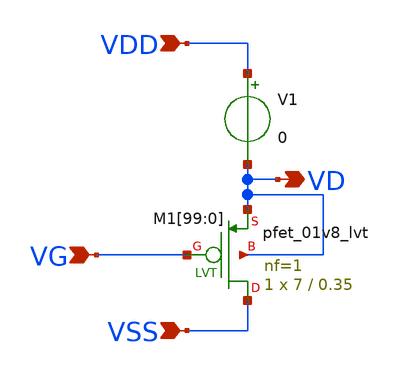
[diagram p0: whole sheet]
** sch_path: design/THESIS_EXP_RO_INVERTER_SKY130A/TB_FET.sch
**.subckt TB_FET VDD VSS VD VG
*.ipin VDD
*.ipin VSS
*.opin VD
*.ipin VG
V1 VDD VD 0
.save i(v1)
XM1[99] VSS VG VD VD sky130_fd_pr__pfet_01v8_lvt L=0.35 W=7 nf=1 ad='int((1 + 1)/2) * 7 / 1 * 0.29' as='int((1 + 2)/2) * 7 / 1 * 0.29'
+ pd='2*int((1 + 1)/2) * (7 / 1 + 0.29)' ps='2*int((1 + 2)/2) * (7 / 1 + 0.29)' nrd='0.29 / 7 ' nrs='0.29 / 7 '
+ sa=0 sb=0 sd=0 mult=1 m=1
XM1[98] VSS VG VD VD sky130_fd_pr__pfet_01v8_lvt L=0.35 W=7 nf=1 ad='int((1 + 1)/2) * 7 / 1 * 0.29' as='int((1 + 2)/2) * 7 / 1 * 0.29'
+ pd='2*int((1 + 1)/2) * (7 / 1 + 0.29)' ps='2*int((1 + 2)/2) * (7 / 1 + 0.29)' nrd='0.29 / 7 ' nrs='0.29 / 7 '
+ sa=0 sb=0 sd=0 mult=1 m=1
XM1[97] VSS VG VD VD sky130_fd_pr__pfet_01v8_lvt L=0.35 W=7 nf=1 ad='int((1 + 1)/2) * 7 / 1 * 0.29' as='int((1 + 2)/2) * 7 / 1 * 0.29'
+ pd='2*int((1 + 1)/2) * (7 / 1 + 0.29)' ps='2*int((1 + 2)/2) * (7 / 1 + 0.29)' nrd='0.29 / 7 ' nrs='0.29 / 7 '
+ sa=0 sb=0 sd=0 mult=1 m=1
XM1[96] VSS VG VD VD sky130_fd_pr__pfet_01v8_lvt L=0.35 W=7 nf=1 ad='int((1 + 1)/2) * 7 / 1 * 0.29' as='int((1 + 2)/2) * 7 / 1 * 0.29'
+ pd='2*int((1 + 1)/2) * (7 / 1 + 0.29)' ps='2*int((1 + 2)/2) * (7 / 1 + 0.29)' nrd='0.29 / 7 ' nrs='0.29 / 7 '
+ sa=0 sb=0 sd=0 mult=1 m=1
XM1[95] VSS VG VD VD sky130_fd_pr__pfet_01v8_lvt L=0.35 W=7 nf=1 ad='int((1 + 1)/2) * 7 / 1 * 0.29' as='int((1 + 2)/2) * 7 / 1 * 0.29'
+ pd='2*int((1 + 1)/2) * (7 / 1 + 0.29)' ps='2*int((1 + 2)/2) * (7 / 1 + 0.29)' nrd='0.29 / 7 ' nrs='0.29 / 7 '
+ sa=0 sb=0 sd=0 mult=1 m=1
XM1[94] VSS VG VD VD sky130_fd_pr__pfet_01v8_lvt L=0.35 W=7 nf=1 ad='int((1 + 1)/2) * 7 / 1 * 0.29' as='int((1 + 2)/2) * 7 / 1 * 0.29'
+ pd='2*int((1 + 1)/2) * (7 / 1 + 0.29)' ps='2*int((1 + 2)/2) * (7 / 1 + 0.29)' nrd='0.29 / 7 ' nrs='0.29 / 7 '
+ sa=0 sb=0 sd=0 mult=1 m=1
XM1[93] VSS VG VD VD sky130_fd_pr__pfet_01v8_lvt L=0.35 W=7 nf=1 ad='int((1 + 1)/2) * 7 / 1 * 0.29' as='int((1 + 2)/2) * 7 / 1 * 0.29'
+ pd='2*int((1 + 1)/2) * (7 / 1 + 0.29)' ps='2*int((1 + 2)/2) * (7 / 1 + 0.29)' nrd='0.29 / 7 ' nrs='0.29 / 7 '
+ sa=0 sb=0 sd=0 mult=1 m=1
XM1[92] VSS VG VD VD sky130_fd_pr__pfet_01v8_lvt L=0.35 W=7 nf=1 ad='int((1 + 1)/2) * 7 / 1 * 0.29' as='int((1 + 2)/2) * 7 / 1 * 0.29'
+ pd='2*int((1 + 1)/2) * (7 / 1 + 0.29)' ps='2*int((1 + 2)/2) * (7 / 1 + 0.29)' nrd='0.29 / 7 ' nrs='0.29 / 7 '
+ sa=0 sb=0 sd=0 mult=1 m=1
XM1[91] VSS VG VD VD sky130_fd_pr__pfet_01v8_lvt L=0.35 W=7 nf=1 ad='int((1 + 1)/2) * 7 / 1 * 0.29' as='int((1 + 2)/2) * 7 / 1 * 0.29'
+ pd='2*int((1 + 1)/2) * (7 / 1 + 0.29)' ps='2*int((1 + 2)/2) * (7 / 1 + 0.29)' nrd='0.29 / 7 ' nrs='0.29 / 7 '
+ sa=0 sb=0 sd=0 mult=1 m=1
XM1[90] VSS VG VD VD sky130_fd_pr__pfet_01v8_lvt L=0.35 W=7 nf=1 ad='int((1 + 1)/2) * 7 / 1 * 0.29' as='int((1 + 2)/2) * 7 / 1 * 0.29'
+ pd='2*int((1 + 1)/2) * (7 / 1 + 0.29)' ps='2*int((1 + 2)/2) * (7 / 1 + 0.29)' nrd='0.29 / 7 ' nrs='0.29 / 7 '
+ sa=0 sb=0 sd=0 mult=1 m=1
XM1[89] VSS VG VD VD sky130_fd_pr__pfet_01v8_lvt L=0.35 W=7 nf=1 ad='int((1 + 1)/2) * 7 / 1 * 0.29' as='int((1 + 2)/2) * 7 / 1 * 0.29'
+ pd='2*int((1 + 1)/2) * (7 / 1 + 0.29)' ps='2*int((1 + 2)/2) * (7 / 1 + 0.29)' nrd='0.29 / 7 ' nrs='0.29 / 7 '
+ sa=0 sb=0 sd=0 mult=1 m=1
XM1[88] VSS VG VD VD sky130_fd_pr__pfet_01v8_lvt L=0.35 W=7 nf=1 ad='int((1 + 1)/2) * 7 / 1 * 0.29' as='int((1 + 2)/2) * 7 / 1 * 0.29'
+ pd='2*int((1 + 1)/2) * (7 / 1 + 0.29)' ps='2*int((1 + 2)/2) * (7 / 1 + 0.29)' nrd='0.29 / 7 ' nrs='0.29 / 7 '
+ sa=0 sb=0 sd=0 mult=1 m=1
XM1[87] VSS VG VD VD sky130_fd_pr__pfet_01v8_lvt L=0.35 W=7 nf=1 ad='int((1 + 1)/2) * 7 / 1 * 0.29' as='int((1 + 2)/2) * 7 / 1 * 0.29'
+ pd='2*int((1 + 1)/2) * (7 / 1 + 0.29)' ps='2*int((1 + 2)/2) * (7 / 1 + 0.29)' nrd='0.29 / 7 ' nrs='0.29 / 7 '
+ sa=0 sb=0 sd=0 mult=1 m=1
XM1[86] VSS VG VD VD sky130_fd_pr__pfet_01v8_lvt L=0.35 W=7 nf=1 ad='int((1 + 1)/2) * 7 / 1 * 0.29' as='int((1 + 2)/2) * 7 / 1 * 0.29'
+ pd='2*int((1 + 1)/2) * (7 / 1 + 0.29)' ps='2*int((1 + 2)/2) * (7 / 1 + 0.29)' nrd='0.29 / 7 ' nrs='0.29 / 7 '
+ sa=0 sb=0 sd=0 mult=1 m=1
XM1[85] VSS VG VD VD sky130_fd_pr__pfet_01v8_lvt L=0.35 W=7 nf=1 ad='int((1 + 1)/2) * 7 / 1 * 0.29' as='int((1 + 2)/2) * 7 / 1 * 0.29'
+ pd='2*int((1 + 1)/2) * (7 / 1 + 0.29)' ps='2*int((1 + 2)/2) * (7 / 1 + 0.29)' nrd='0.29 / 7 ' nrs='0.29 / 7 '
+ sa=0 sb=0 sd=0 mult=1 m=1
XM1[84] VSS VG VD VD sky130_fd_pr__pfet_01v8_lvt L=0.35 W=7 nf=1 ad='int((1 + 1)/2) * 7 / 1 * 0.29' as='int((1 + 2)/2) * 7 / 1 * 0.29'
+ pd='2*int((1 + 1)/2) * (7 / 1 + 0.29)' ps='2*int((1 + 2)/2) * (7 / 1 + 0.29)' nrd='0.29 / 7 ' nrs='0.29 / 7 '
+ sa=0 sb=0 sd=0 mult=1 m=1
XM1[83] VSS VG VD VD sky130_fd_pr__pfet_01v8_lvt L=0.35 W=7 nf=1 ad='int((1 + 1)/2) * 7 / 1 * 0.29' as='int((1 + 2)/2) * 7 / 1 * 0.29'
+ pd='2*int((1 + 1)/2) * (7 / 1 + 0.29)' ps='2*int((1 + 2)/2) * (7 / 1 + 0.29)' nrd='0.29 / 7 ' nrs='0.29 / 7 '
+ sa=0 sb=0 sd=0 mult=1 m=1
XM1[82] VSS VG VD VD sky130_fd_pr__pfet_01v8_lvt L=0.35 W=7 nf=1 ad='int((1 + 1)/2) * 7 / 1 * 0.29' as='int((1 + 2)/2) * 7 / 1 * 0.29'
+ pd='2*int((1 + 1)/2) * (7 / 1 + 0.29)' ps='2*int((1 + 2)/2) * (7 / 1 + 0.29)' nrd='0.29 / 7 ' nrs='0.29 / 7 '
+ sa=0 sb=0 sd=0 mult=1 m=1
XM1[81] VSS VG VD VD sky130_fd_pr__pfet_01v8_lvt L=0.35 W=7 nf=1 ad='int((1 + 1)/2) * 7 / 1 * 0.29' as='int((1 + 2)/2) * 7 / 1 * 0.29'
+ pd='2*int((1 + 1)/2) * (7 / 1 + 0.29)' ps='2*int((1 + 2)/2) * (7 / 1 + 0.29)' nrd='0.29 / 7 ' nrs='0.29 / 7 '
+ sa=0 sb=0 sd=0 mult=1 m=1
XM1[80] VSS VG VD VD sky130_fd_pr__pfet_01v8_lvt L=0.35 W=7 nf=1 ad='int((1 + 1)/2) * 7 / 1 * 0.29' as='int((1 + 2)/2) * 7 / 1 * 0.29'
+ pd='2*int((1 + 1)/2) * (7 / 1 + 0.29)' ps='2*int((1 + 2)/2) * (7 / 1 + 0.29)' nrd='0.29 / 7 ' nrs='0.29 / 7 '
+ sa=0 sb=0 sd=0 mult=1 m=1
XM1[79] VSS VG VD VD sky130_fd_pr__pfet_01v8_lvt L=0.35 W=7 nf=1 ad='int((1 + 1)/2) * 7 / 1 * 0.29' as='int((1 + 2)/2) * 7 / 1 * 0.29'
+ pd='2*int((1 + 1)/2) * (7 / 1 + 0.29)' ps='2*int((1 + 2)/2) * (7 / 1 + 0.29)' nrd='0.29 / 7 ' nrs='0.29 / 7 '
+ sa=0 sb=0 sd=0 mult=1 m=1
XM1[78] VSS VG VD VD sky130_fd_pr__pfet_01v8_lvt L=0.35 W=7 nf=1 ad='int((1 + 1)/2) * 7 / 1 * 0.29' as='int((1 + 2)/2) * 7 / 1 * 0.29'
+ pd='2*int((1 + 1)/2) * (7 / 1 + 0.29)' ps='2*int((1 + 2)/2) * (7 / 1 + 0.29)' nrd='0.29 / 7 ' nrs='0.29 / 7 '
+ sa=0 sb=0 sd=0 mult=1 m=1
XM1[77] VSS VG VD VD sky130_fd_pr__pfet_01v8_lvt L=0.35 W=7 nf=1 ad='int((1 + 1)/2) * 7 / 1 * 0.29' as='int((1 + 2)/2) * 7 / 1 * 0.29'
+ pd='2*int((1 + 1)/2) * (7 / 1 + 0.29)' ps='2*int((1 + 2)/2) * (7 / 1 + 0.29)' nrd='0.29 / 7 ' nrs='0.29 / 7 '
+ sa=0 sb=0 sd=0 mult=1 m=1
XM1[76] VSS VG VD VD sky130_fd_pr__pfet_01v8_lvt L=0.35 W=7 nf=1 ad='int((1 + 1)/2) * 7 / 1 * 0.29' as='int((1 + 2)/2) * 7 / 1 * 0.29'
+ pd='2*int((1 + 1)/2) * (7 / 1 + 0.29)' ps='2*int((1 + 2)/2) * (7 / 1 + 0.29)' nrd='0.29 / 7 ' nrs='0.29 / 7 '
+ sa=0 sb=0 sd=0 mult=1 m=1
XM1[75] VSS VG VD VD sky130_fd_pr__pfet_01v8_lvt L=0.35 W=7 nf=1 ad='int((1 + 1)/2) * 7 / 1 * 0.29' as='int((1 + 2)/2) * 7 / 1 * 0.29'
+ pd='2*int((1 + 1)/2) * (7 / 1 + 0.29)' ps='2*int((1 + 2)/2) * (7 / 1 + 0.29)' nrd='0.29 / 7 ' nrs='0.29 / 7 '
+ sa=0 sb=0 sd=0 mult=1 m=1
XM1[74] VSS VG VD VD sky130_fd_pr__pfet_01v8_lvt L=0.35 W=7 nf=1 ad='int((1 + 1)/2) * 7 / 1 * 0.29' as='int((1 + 2)/2) * 7 / 1 * 0.29'
+ pd='2*int((1 + 1)/2) * (7 / 1 + 0.29)' ps='2*int((1 + 2)/2) * (7 / 1 + 0.29)' nrd='0.29 / 7 ' nrs='0.29 / 7 '
+ sa=0 sb=0 sd=0 mult=1 m=1
XM1[73] VSS VG VD VD sky130_fd_pr__pfet_01v8_lvt L=0.35 W=7 nf=1 ad='int((1 + 1)/2) * 7 / 1 * 0.29' as='int((1 + 2)/2) * 7 / 1 * 0.29'
+ pd='2*int((1 + 1)/2) * (7 / 1 + 0.29)' ps='2*int((1 + 2)/2) * (7 / 1 + 0.29)' nrd='0.29 / 7 ' nrs='0.29 / 7 '
+ sa=0 sb=0 sd=0 mult=1 m=1
XM1[72] VSS VG VD VD sky130_fd_pr__pfet_01v8_lvt L=0.35 W=7 nf=1 ad='int((1 + 1)/2) * 7 / 1 * 0.29' as='int((1 + 2)/2) * 7 / 1 * 0.29'
+ pd='2*int((1 + 1)/2) * (7 / 1 + 0.29)' ps='2*int((1 + 2)/2) * (7 / 1 + 0.29)' nrd='0.29 / 7 ' nrs='0.29 / 7 '
+ sa=0 sb=0 sd=0 mult=1 m=1
XM1[71] VSS VG VD VD sky130_fd_pr__pfet_01v8_lvt L=0.35 W=7 nf=1 ad='int((1 + 1)/2) * 7 / 1 * 0.29' as='int((1 + 2)/2) * 7 / 1 * 0.29'
+ pd='2*int((1 + 1)/2) * (7 / 1 + 0.29)' ps='2*int((1 + 2)/2) * (7 / 1 + 0.29)' nrd='0.29 / 7 ' nrs='0.29 / 7 '
+ sa=0 sb=0 sd=0 mult=1 m=1
XM1[70] VSS VG VD VD sky130_fd_pr__pfet_01v8_lvt L=0.35 W=7 nf=1 ad='int((1 + 1)/2) * 7 / 1 * 0.29' as='int((1 + 2)/2) * 7 / 1 * 0.29'
+ pd='2*int((1 + 1)/2) * (7 / 1 + 0.29)' ps='2*int((1 + 2)/2) * (7 / 1 + 0.29)' nrd='0.29 / 7 ' nrs='0.29 / 7 '
+ sa=0 sb=0 sd=0 mult=1 m=1
XM1[69] VSS VG VD VD sky130_fd_pr__pfet_01v8_lvt L=0.35 W=7 nf=1 ad='int((1 + 1)/2) * 7 / 1 * 0.29' as='int((1 + 2)/2) * 7 / 1 * 0.29'
+ pd='2*int((1 + 1)/2) * (7 / 1 + 0.29)' ps='2*int((1 + 2)/2) * (7 / 1 + 0.29)' nrd='0.29 / 7 ' nrs='0.29 / 7 '
+ sa=0 sb=0 sd=0 mult=1 m=1
XM1[68] VSS VG VD VD sky130_fd_pr__pfet_01v8_lvt L=0.35 W=7 nf=1 ad='int((1 + 1)/2) * 7 / 1 * 0.29' as='int((1 + 2)/2) * 7 / 1 * 0.29'
+ pd='2*int((1 + 1)/2) * (7 / 1 + 0.29)' ps='2*int((1 + 2)/2) * (7 / 1 + 0.29)' nrd='0.29 / 7 ' nrs='0.29 / 7 '
+ sa=0 sb=0 sd=0 mult=1 m=1
XM1[67] VSS VG VD VD sky130_fd_pr__pfet_01v8_lvt L=0.35 W=7 nf=1 ad='int((1 + 1)/2) * 7 / 1 * 0.29' as='int((1 + 2)/2) * 7 / 1 * 0.29'
+ pd='2*int((1 + 1)/2) * (7 / 1 + 0.29)' ps='2*int((1 + 2)/2) * (7 / 1 + 0.29)' nrd='0.29 / 7 ' nrs='0.29 / 7 '
+ sa=0 sb=0 sd=0 mult=1 m=1
XM1[66] VSS VG VD VD sky130_fd_pr__pfet_01v8_lvt L=0.35 W=7 nf=1 ad='int((1 + 1)/2) * 7 / 1 * 0.29' as='int((1 + 2)/2) * 7 / 1 * 0.29'
+ pd='2*int((1 + 1)/2) * (7 / 1 + 0.29)' ps='2*int((1 + 2)/2) * (7 / 1 + 0.29)' nrd='0.29 / 7 ' nrs='0.29 / 7 '
+ sa=0 sb=0 sd=0 mult=1 m=1
XM1[65] VSS VG VD VD sky130_fd_pr__pfet_01v8_lvt L=0.35 W=7 nf=1 ad='int((1 + 1)/2) * 7 / 1 * 0.29' as='int((1 + 2)/2) * 7 / 1 * 0.29'
+ pd='2*int((1 + 1)/2) * (7 / 1 + 0.29)' ps='2*int((1 + 2)/2) * (7 / 1 + 0.29)' nrd='0.29 / 7 ' nrs='0.29 / 7 '
+ sa=0 sb=0 sd=0 mult=1 m=1
XM1[64] VSS VG VD VD sky130_fd_pr__pfet_01v8_lvt L=0.35 W=7 nf=1 ad='int((1 + 1)/2) * 7 / 1 * 0.29' as='int((1 + 2)/2) * 7 / 1 * 0.29'
+ pd='2*int((1 + 1)/2) * (7 / 1 + 0.29)' ps='2*int((1 + 2)/2) * (7 / 1 + 0.29)' nrd='0.29 / 7 ' nrs='0.29 / 7 '
+ sa=0 sb=0 sd=0 mult=1 m=1
XM1[63] VSS VG VD VD sky130_fd_pr__pfet_01v8_lvt L=0.35 W=7 nf=1 ad='int((1 + 1)/2) * 7 / 1 * 0.29' as='int((1 + 2)/2) * 7 / 1 * 0.29'
+ pd='2*int((1 + 1)/2) * (7 / 1 + 0.29)' ps='2*int((1 + 2)/2) * (7 / 1 + 0.29)' nrd='0.29 / 7 ' nrs='0.29 / 7 '
+ sa=0 sb=0 sd=0 mult=1 m=1
XM1[62] VSS VG VD VD sky130_fd_pr__pfet_01v8_lvt L=0.35 W=7 nf=1 ad='int((1 + 1)/2) * 7 / 1 * 0.29' as='int((1 + 2)/2) * 7 / 1 * 0.29'
+ pd='2*int((1 + 1)/2) * (7 / 1 + 0.29)' ps='2*int((1 + 2)/2) * (7 / 1 + 0.29)' nrd='0.29 / 7 ' nrs='0.29 / 7 '
+ sa=0 sb=0 sd=0 mult=1 m=1
XM1[61] VSS VG VD VD sky130_fd_pr__pfet_01v8_lvt L=0.35 W=7 nf=1 ad='int((1 + 1)/2) * 7 / 1 * 0.29' as='int((1 + 2)/2) * 7 / 1 * 0.29'
+ pd='2*int((1 + 1)/2) * (7 / 1 + 0.29)' ps='2*int((1 + 2)/2) * (7 / 1 + 0.29)' nrd='0.29 / 7 ' nrs='0.29 / 7 '
+ sa=0 sb=0 sd=0 mult=1 m=1
XM1[60] VSS VG VD VD sky130_fd_pr__pfet_01v8_lvt L=0.35 W=7 nf=1 ad='int((1 + 1)/2) * 7 / 1 * 0.29' as='int((1 + 2)/2) * 7 / 1 * 0.29'
+ pd='2*int((1 + 1)/2) * (7 / 1 + 0.29)' ps='2*int((1 + 2)/2) * (7 / 1 + 0.29)' nrd='0.29 / 7 ' nrs='0.29 / 7 '
+ sa=0 sb=0 sd=0 mult=1 m=1
XM1[59] VSS VG VD VD sky130_fd_pr__pfet_01v8_lvt L=0.35 W=7 nf=1 ad='int((1 + 1)/2) * 7 / 1 * 0.29' as='int((1 + 2)/2) * 7 / 1 * 0.29'
+ pd='2*int((1 + 1)/2) * (7 / 1 + 0.29)' ps='2*int((1 + 2)/2) * (7 / 1 + 0.29)' nrd='0.29 / 7 ' nrs='0.29 / 7 '
+ sa=0 sb=0 sd=0 mult=1 m=1
XM1[58] VSS VG VD VD sky130_fd_pr__pfet_01v8_lvt L=0.35 W=7 nf=1 ad='int((1 + 1)/2) * 7 / 1 * 0.29' as='int((1 + 2)/2) * 7 / 1 * 0.29'
+ pd='2*int((1 + 1)/2) * (7 / 1 + 0.29)' ps='2*int((1 + 2)/2) * (7 / 1 + 0.29)' nrd='0.29 / 7 ' nrs='0.29 / 7 '
+ sa=0 sb=0 sd=0 mult=1 m=1
XM1[57] VSS VG VD VD sky130_fd_pr__pfet_01v8_lvt L=0.35 W=7 nf=1 ad='int((1 + 1)/2) * 7 / 1 * 0.29' as='int((1 + 2)/2) * 7 / 1 * 0.29'
+ pd='2*int((1 + 1)/2) * (7 / 1 + 0.29)' ps='2*int((1 + 2)/2) * (7 / 1 + 0.29)' nrd='0.29 / 7 ' nrs='0.29 / 7 '
+ sa=0 sb=0 sd=0 mult=1 m=1
XM1[56] VSS VG VD VD sky130_fd_pr__pfet_01v8_lvt L=0.35 W=7 nf=1 ad='int((1 + 1)/2) * 7 / 1 * 0.29' as='int((1 + 2)/2) * 7 / 1 * 0.29'
+ pd='2*int((1 + 1)/2) * (7 / 1 + 0.29)' ps='2*int((1 + 2)/2) * (7 / 1 + 0.29)' nrd='0.29 / 7 ' nrs='0.29 / 7 '
+ sa=0 sb=0 sd=0 mult=1 m=1
XM1[55] VSS VG VD VD sky130_fd_pr__pfet_01v8_lvt L=0.35 W=7 nf=1 ad='int((1 + 1)/2) * 7 / 1 * 0.29' as='int((1 + 2)/2) * 7 / 1 * 0.29'
+ pd='2*int((1 + 1)/2) * (7 / 1 + 0.29)' ps='2*int((1 + 2)/2) * (7 / 1 + 0.29)' nrd='0.29 / 7 ' nrs='0.29 / 7 '
+ sa=0 sb=0 sd=0 mult=1 m=1
XM1[54] VSS VG VD VD sky130_fd_pr__pfet_01v8_lvt L=0.35 W=7 nf=1 ad='int((1 + 1)/2) * 7 / 1 * 0.29' as='int((1 + 2)/2) * 7 / 1 * 0.29'
+ pd='2*int((1 + 1)/2) * (7 / 1 + 0.29)' ps='2*int((1 + 2)/2) * (7 / 1 + 0.29)' nrd='0.29 / 7 ' nrs='0.29 / 7 '
+ sa=0 sb=0 sd=0 mult=1 m=1
XM1[53] VSS VG VD VD sky130_fd_pr__pfet_01v8_lvt L=0.35 W=7 nf=1 ad='int((1 + 1)/2) * 7 / 1 * 0.29' as='int((1 + 2)/2) * 7 / 1 * 0.29'
+ pd='2*int((1 + 1)/2) * (7 / 1 + 0.29)' ps='2*int((1 + 2)/2) * (7 / 1 + 0.29)' nrd='0.29 / 7 ' nrs='0.29 / 7 '
+ sa=0 sb=0 sd=0 mult=1 m=1
XM1[52] VSS VG VD VD sky130_fd_pr__pfet_01v8_lvt L=0.35 W=7 nf=1 ad='int((1 + 1)/2) * 7 / 1 * 0.29' as='int((1 + 2)/2) * 7 / 1 * 0.29'
+ pd='2*int((1 + 1)/2) * (7 / 1 + 0.29)' ps='2*int((1 + 2)/2) * (7 / 1 + 0.29)' nrd='0.29 / 7 ' nrs='0.29 / 7 '
+ sa=0 sb=0 sd=0 mult=1 m=1
XM1[51] VSS VG VD VD sky130_fd_pr__pfet_01v8_lvt L=0.35 W=7 nf=1 ad='int((1 + 1)/2) * 7 / 1 * 0.29' as='int((1 + 2)/2) * 7 / 1 * 0.29'
+ pd='2*int((1 + 1)/2) * (7 / 1 + 0.29)' ps='2*int((1 + 2)/2) * (7 / 1 + 0.29)' nrd='0.29 / 7 ' nrs='0.29 / 7 '
+ sa=0 sb=0 sd=0 mult=1 m=1
XM1[50] VSS VG VD VD sky130_fd_pr__pfet_01v8_lvt L=0.35 W=7 nf=1 ad='int((1 + 1)/2) * 7 / 1 * 0.29' as='int((1 + 2)/2) * 7 / 1 * 0.29'
+ pd='2*int((1 + 1)/2) * (7 / 1 + 0.29)' ps='2*int((1 + 2)/2) * (7 / 1 + 0.29)' nrd='0.29 / 7 ' nrs='0.29 / 7 '
+ sa=0 sb=0 sd=0 mult=1 m=1
XM1[49] VSS VG VD VD sky130_fd_pr__pfet_01v8_lvt L=0.35 W=7 nf=1 ad='int((1 + 1)/2) * 7 / 1 * 0.29' as='int((1 + 2)/2) * 7 / 1 * 0.29'
+ pd='2*int((1 + 1)/2) * (7 / 1 + 0.29)' ps='2*int((1 + 2)/2) * (7 / 1 + 0.29)' nrd='0.29 / 7 ' nrs='0.29 / 7 '
+ sa=0 sb=0 sd=0 mult=1 m=1
XM1[48] VSS VG VD VD sky130_fd_pr__pfet_01v8_lvt L=0.35 W=7 nf=1 ad='int((1 + 1)/2) * 7 / 1 * 0.29' as='int((1 + 2)/2) * 7 / 1 * 0.29'
+ pd='2*int((1 + 1)/2) * (7 / 1 + 0.29)' ps='2*int((1 + 2)/2) * (7 / 1 + 0.29)' nrd='0.29 / 7 ' nrs='0.29 / 7 '
+ sa=0 sb=0 sd=0 mult=1 m=1
XM1[47] VSS VG VD VD sky130_fd_pr__pfet_01v8_lvt L=0.35 W=7 nf=1 ad='int((1 + 1)/2) * 7 / 1 * 0.29' as='int((1 + 2)/2) * 7 / 1 * 0.29'
+ pd='2*int((1 + 1)/2) * (7 / 1 + 0.29)' ps='2*int((1 + 2)/2) * (7 / 1 + 0.29)' nrd='0.29 / 7 ' nrs='0.29 / 7 '
+ sa=0 sb=0 sd=0 mult=1 m=1
XM1[46] VSS VG VD VD sky130_fd_pr__pfet_01v8_lvt L=0.35 W=7 nf=1 ad='int((1 + 1)/2) * 7 / 1 * 0.29' as='int((1 + 2)/2) * 7 / 1 * 0.29'
+ pd='2*int((1 + 1)/2) * (7 / 1 + 0.29)' ps='2*int((1 + 2)/2) * (7 / 1 + 0.29)' nrd='0.29 / 7 ' nrs='0.29 / 7 '
+ sa=0 sb=0 sd=0 mult=1 m=1
XM1[45] VSS VG VD VD sky130_fd_pr__pfet_01v8_lvt L=0.35 W=7 nf=1 ad='int((1 + 1)/2) * 7 / 1 * 0.29' as='int((1 + 2)/2) * 7 / 1 * 0.29'
+ pd='2*int((1 + 1)/2) * (7 / 1 + 0.29)' ps='2*int((1 + 2)/2) * (7 / 1 + 0.29)' nrd='0.29 / 7 ' nrs='0.29 / 7 '
+ sa=0 sb=0 sd=0 mult=1 m=1
XM1[44] VSS VG VD VD sky130_fd_pr__pfet_01v8_lvt L=0.35 W=7 nf=1 ad='int((1 + 1)/2) * 7 / 1 * 0.29' as='int((1 + 2)/2) * 7 / 1 * 0.29'
+ pd='2*int((1 + 1)/2) * (7 / 1 + 0.29)' ps='2*int((1 + 2)/2) * (7 / 1 + 0.29)' nrd='0.29 / 7 ' nrs='0.29 / 7 '
+ sa=0 sb=0 sd=0 mult=1 m=1
XM1[43] VSS VG VD VD sky130_fd_pr__pfet_01v8_lvt L=0.35 W=7 nf=1 ad='int((1 + 1)/2) * 7 / 1 * 0.29' as='int((1 + 2)/2) * 7 / 1 * 0.29'
+ pd='2*int((1 + 1)/2) * (7 / 1 + 0.29)' ps='2*int((1 + 2)/2) * (7 / 1 + 0.29)' nrd='0.29 / 7 ' nrs='0.29 / 7 '
+ sa=0 sb=0 sd=0 mult=1 m=1
XM1[42] VSS VG VD VD sky130_fd_pr__pfet_01v8_lvt L=0.35 W=7 nf=1 ad='int((1 + 1)/2) * 7 / 1 * 0.29' as='int((1 + 2)/2) * 7 / 1 * 0.29'
+ pd='2*int((1 + 1)/2) * (7 / 1 + 0.29)' ps='2*int((1 + 2)/2) * (7 / 1 + 0.29)' nrd='0.29 / 7 ' nrs='0.29 / 7 '
+ sa=0 sb=0 sd=0 mult=1 m=1
XM1[41] VSS VG VD VD sky130_fd_pr__pfet_01v8_lvt L=0.35 W=7 nf=1 ad='int((1 + 1)/2) * 7 / 1 * 0.29' as='int((1 + 2)/2) * 7 / 1 * 0.29'
+ pd='2*int((1 + 1)/2) * (7 / 1 + 0.29)' ps='2*int((1 + 2)/2) * (7 / 1 + 0.29)' nrd='0.29 / 7 ' nrs='0.29 / 7 '
+ sa=0 sb=0 sd=0 mult=1 m=1
XM1[40] VSS VG VD VD sky130_fd_pr__pfet_01v8_lvt L=0.35 W=7 nf=1 ad='int((1 + 1)/2) * 7 / 1 * 0.29' as='int((1 + 2)/2) * 7 / 1 * 0.29'
+ pd='2*int((1 + 1)/2) * (7 / 1 + 0.29)' ps='2*int((1 + 2)/2) * (7 / 1 + 0.29)' nrd='0.29 / 7 ' nrs='0.29 / 7 '
+ sa=0 sb=0 sd=0 mult=1 m=1
XM1[39] VSS VG VD VD sky130_fd_pr__pfet_01v8_lvt L=0.35 W=7 nf=1 ad='int((1 + 1)/2) * 7 / 1 * 0.29' as='int((1 + 2)/2) * 7 / 1 * 0.29'
+ pd='2*int((1 + 1)/2) * (7 / 1 + 0.29)' ps='2*int((1 + 2)/2) * (7 / 1 + 0.29)' nrd='0.29 / 7 ' nrs='0.29 / 7 '
+ sa=0 sb=0 sd=0 mult=1 m=1
XM1[38] VSS VG VD VD sky130_fd_pr__pfet_01v8_lvt L=0.35 W=7 nf=1 ad='int((1 + 1)/2) * 7 / 1 * 0.29' as='int((1 + 2)/2) * 7 / 1 * 0.29'
+ pd='2*int((1 + 1)/2) * (7 / 1 + 0.29)' ps='2*int((1 + 2)/2) * (7 / 1 + 0.29)' nrd='0.29 / 7 ' nrs='0.29 / 7 '
+ sa=0 sb=0 sd=0 mult=1 m=1
XM1[37] VSS VG VD VD sky130_fd_pr__pfet_01v8_lvt L=0.35 W=7 nf=1 ad='int((1 + 1)/2) * 7 / 1 * 0.29' as='int((1 + 2)/2) * 7 / 1 * 0.29'
+ pd='2*int((1 + 1)/2) * (7 / 1 + 0.29)' ps='2*int((1 + 2)/2) * (7 / 1 + 0.29)' nrd='0.29 / 7 ' nrs='0.29 / 7 '
+ sa=0 sb=0 sd=0 mult=1 m=1
XM1[36] VSS VG VD VD sky130_fd_pr__pfet_01v8_lvt L=0.35 W=7 nf=1 ad='int((1 + 1)/2) * 7 / 1 * 0.29' as='int((1 + 2)/2) * 7 / 1 * 0.29'
+ pd='2*int((1 + 1)/2) * (7 / 1 + 0.29)' ps='2*int((1 + 2)/2) * (7 / 1 + 0.29)' nrd='0.29 / 7 ' nrs='0.29 / 7 '
+ sa=0 sb=0 sd=0 mult=1 m=1
XM1[35] VSS VG VD VD sky130_fd_pr__pfet_01v8_lvt L=0.35 W=7 nf=1 ad='int((1 + 1)/2) * 7 / 1 * 0.29' as='int((1 + 2)/2) * 7 / 1 * 0.29'
+ pd='2*int((1 + 1)/2) * (7 / 1 + 0.29)' ps='2*int((1 + 2)/2) * (7 / 1 + 0.29)' nrd='0.29 / 7 ' nrs='0.29 / 7 '
+ sa=0 sb=0 sd=0 mult=1 m=1
XM1[34] VSS VG VD VD sky130_fd_pr__pfet_01v8_lvt L=0.35 W=7 nf=1 ad='int((1 + 1)/2) * 7 / 1 * 0.29' as='int((1 + 2)/2) * 7 / 1 * 0.29'
+ pd='2*int((1 + 1)/2) * (7 / 1 + 0.29)' ps='2*int((1 + 2)/2) * (7 / 1 + 0.29)' nrd='0.29 / 7 ' nrs='0.29 / 7 '
+ sa=0 sb=0 sd=0 mult=1 m=1
XM1[33] VSS VG VD VD sky130_fd_pr__pfet_01v8_lvt L=0.35 W=7 nf=1 ad='int((1 + 1)/2) * 7 / 1 * 0.29' as='int((1 + 2)/2) * 7 / 1 * 0.29'
+ pd='2*int((1 + 1)/2) * (7 / 1 + 0.29)' ps='2*int((1 + 2)/2) * (7 / 1 + 0.29)' nrd='0.29 / 7 ' nrs='0.29 / 7 '
+ sa=0 sb=0 sd=0 mult=1 m=1
XM1[32] VSS VG VD VD sky130_fd_pr__pfet_01v8_lvt L=0.35 W=7 nf=1 ad='int((1 + 1)/2) * 7 / 1 * 0.29' as='int((1 + 2)/2) * 7 / 1 * 0.29'
+ pd='2*int((1 + 1)/2) * (7 / 1 + 0.29)' ps='2*int((1 + 2)/2) * (7 / 1 + 0.29)' nrd='0.29 / 7 ' nrs='0.29 / 7 '
+ sa=0 sb=0 sd=0 mult=1 m=1
XM1[31] VSS VG VD VD sky130_fd_pr__pfet_01v8_lvt L=0.35 W=7 nf=1 ad='int((1 + 1)/2) * 7 / 1 * 0.29' as='int((1 + 2)/2) * 7 / 1 * 0.29'
+ pd='2*int((1 + 1)/2) * (7 / 1 + 0.29)' ps='2*int((1 + 2)/2) * (7 / 1 + 0.29)' nrd='0.29 / 7 ' nrs='0.29 / 7 '
+ sa=0 sb=0 sd=0 mult=1 m=1
XM1[30] VSS VG VD VD sky130_fd_pr__pfet_01v8_lvt L=0.35 W=7 nf=1 ad='int((1 + 1)/2) * 7 / 1 * 0.29' as='int((1 + 2)/2) * 7 / 1 * 0.29'
+ pd='2*int((1 + 1)/2) * (7 / 1 + 0.29)' ps='2*int((1 + 2)/2) * (7 / 1 + 0.29)' nrd='0.29 / 7 ' nrs='0.29 / 7 '
+ sa=0 sb=0 sd=0 mult=1 m=1
XM1[29] VSS VG VD VD sky130_fd_pr__pfet_01v8_lvt L=0.35 W=7 nf=1 ad='int((1 + 1)/2) * 7 / 1 * 0.29' as='int((1 + 2)/2) * 7 / 1 * 0.29'
+ pd='2*int((1 + 1)/2) * (7 / 1 + 0.29)' ps='2*int((1 + 2)/2) * (7 / 1 + 0.29)' nrd='0.29 / 7 ' nrs='0.29 / 7 '
+ sa=0 sb=0 sd=0 mult=1 m=1
XM1[28] VSS VG VD VD sky130_fd_pr__pfet_01v8_lvt L=0.35 W=7 nf=1 ad='int((1 + 1)/2) * 7 / 1 * 0.29' as='int((1 + 2)/2) * 7 / 1 * 0.29'
+ pd='2*int((1 + 1)/2) * (7 / 1 + 0.29)' ps='2*int((1 + 2)/2) * (7 / 1 + 0.29)' nrd='0.29 / 7 ' nrs='0.29 / 7 '
+ sa=0 sb=0 sd=0 mult=1 m=1
XM1[27] VSS VG VD VD sky130_fd_pr__pfet_01v8_lvt L=0.35 W=7 nf=1 ad='int((1 + 1)/2) * 7 / 1 * 0.29' as='int((1 + 2)/2) * 7 / 1 * 0.29'
+ pd='2*int((1 + 1)/2) * (7 / 1 + 0.29)' ps='2*int((1 + 2)/2) * (7 / 1 + 0.29)' nrd='0.29 / 7 ' nrs='0.29 / 7 '
+ sa=0 sb=0 sd=0 mult=1 m=1
XM1[26] VSS VG VD VD sky130_fd_pr__pfet_01v8_lvt L=0.35 W=7 nf=1 ad='int((1 + 1)/2) * 7 / 1 * 0.29' as='int((1 + 2)/2) * 7 / 1 * 0.29'
+ pd='2*int((1 + 1)/2) * (7 / 1 + 0.29)' ps='2*int((1 + 2)/2) * (7 / 1 + 0.29)' nrd='0.29 / 7 ' nrs='0.29 / 7 '
+ sa=0 sb=0 sd=0 mult=1 m=1
XM1[25] VSS VG VD VD sky130_fd_pr__pfet_01v8_lvt L=0.35 W=7 nf=1 ad='int((1 + 1)/2) * 7 / 1 * 0.29' as='int((1 + 2)/2) * 7 / 1 * 0.29'
+ pd='2*int((1 + 1)/2) * (7 / 1 + 0.29)' ps='2*int((1 + 2)/2) * (7 / 1 + 0.29)' nrd='0.29 / 7 ' nrs='0.29 / 7 '
+ sa=0 sb=0 sd=0 mult=1 m=1
XM1[24] VSS VG VD VD sky130_fd_pr__pfet_01v8_lvt L=0.35 W=7 nf=1 ad='int((1 + 1)/2) * 7 / 1 * 0.29' as='int((1 + 2)/2) * 7 / 1 * 0.29'
+ pd='2*int((1 + 1)/2) * (7 / 1 + 0.29)' ps='2*int((1 + 2)/2) * (7 / 1 + 0.29)' nrd='0.29 / 7 ' nrs='0.29 / 7 '
+ sa=0 sb=0 sd=0 mult=1 m=1
XM1[23] VSS VG VD VD sky130_fd_pr__pfet_01v8_lvt L=0.35 W=7 nf=1 ad='int((1 + 1)/2) * 7 / 1 * 0.29' as='int((1 + 2)/2) * 7 / 1 * 0.29'
+ pd='2*int((1 + 1)/2) * (7 / 1 + 0.29)' ps='2*int((1 + 2)/2) * (7 / 1 + 0.29)' nrd='0.29 / 7 ' nrs='0.29 / 7 '
+ sa=0 sb=0 sd=0 mult=1 m=1
XM1[22] VSS VG VD VD sky130_fd_pr__pfet_01v8_lvt L=0.35 W=7 nf=1 ad='int((1 + 1)/2) * 7 / 1 * 0.29' as='int((1 + 2)/2) * 7 / 1 * 0.29'
+ pd='2*int((1 + 1)/2) * (7 / 1 + 0.29)' ps='2*int((1 + 2)/2) * (7 / 1 + 0.29)' nrd='0.29 / 7 ' nrs='0.29 / 7 '
+ sa=0 sb=0 sd=0 mult=1 m=1
XM1[21] VSS VG VD VD sky130_fd_pr__pfet_01v8_lvt L=0.35 W=7 nf=1 ad='int((1 + 1)/2) * 7 / 1 * 0.29' as='int((1 + 2)/2) * 7 / 1 * 0.29'
+ pd='2*int((1 + 1)/2) * (7 / 1 + 0.29)' ps='2*int((1 + 2)/2) * (7 / 1 + 0.29)' nrd='0.29 / 7 ' nrs='0.29 / 7 '
+ sa=0 sb=0 sd=0 mult=1 m=1
XM1[20] VSS VG VD VD sky130_fd_pr__pfet_01v8_lvt L=0.35 W=7 nf=1 ad='int((1 + 1)/2) * 7 / 1 * 0.29' as='int((1 + 2)/2) * 7 / 1 * 0.29'
+ pd='2*int((1 + 1)/2) * (7 / 1 + 0.29)' ps='2*int((1 + 2)/2) * (7 / 1 + 0.29)' nrd='0.29 / 7 ' nrs='0.29 / 7 '
+ sa=0 sb=0 sd=0 mult=1 m=1
XM1[19] VSS VG VD VD sky130_fd_pr__pfet_01v8_lvt L=0.35 W=7 nf=1 ad='int((1 + 1)/2) * 7 / 1 * 0.29' as='int((1 + 2)/2) * 7 / 1 * 0.29'
+ pd='2*int((1 + 1)/2) * (7 / 1 + 0.29)' ps='2*int((1 + 2)/2) * (7 / 1 + 0.29)' nrd='0.29 / 7 ' nrs='0.29 / 7 '
+ sa=0 sb=0 sd=0 mult=1 m=1
XM1[18] VSS VG VD VD sky130_fd_pr__pfet_01v8_lvt L=0.35 W=7 nf=1 ad='int((1 + 1)/2) * 7 / 1 * 0.29' as='int((1 + 2)/2) * 7 / 1 * 0.29'
+ pd='2*int((1 + 1)/2) * (7 / 1 + 0.29)' ps='2*int((1 + 2)/2) * (7 / 1 + 0.29)' nrd='0.29 / 7 ' nrs='0.29 / 7 '
+ sa=0 sb=0 sd=0 mult=1 m=1
XM1[17] VSS VG VD VD sky130_fd_pr__pfet_01v8_lvt L=0.35 W=7 nf=1 ad='int((1 + 1)/2) * 7 / 1 * 0.29' as='int((1 + 2)/2) * 7 / 1 * 0.29'
+ pd='2*int((1 + 1)/2) * (7 / 1 + 0.29)' ps='2*int((1 + 2)/2) * (7 / 1 + 0.29)' nrd='0.29 / 7 ' nrs='0.29 / 7 '
+ sa=0 sb=0 sd=0 mult=1 m=1
XM1[16] VSS VG VD VD sky130_fd_pr__pfet_01v8_lvt L=0.35 W=7 nf=1 ad='int((1 + 1)/2) * 7 / 1 * 0.29' as='int((1 + 2)/2) * 7 / 1 * 0.29'
+ pd='2*int((1 + 1)/2) * (7 / 1 + 0.29)' ps='2*int((1 + 2)/2) * (7 / 1 + 0.29)' nrd='0.29 / 7 ' nrs='0.29 / 7 '
+ sa=0 sb=0 sd=0 mult=1 m=1
XM1[15] VSS VG VD VD sky130_fd_pr__pfet_01v8_lvt L=0.35 W=7 nf=1 ad='int((1 + 1)/2) * 7 / 1 * 0.29' as='int((1 + 2)/2) * 7 / 1 * 0.29'
+ pd='2*int((1 + 1)/2) * (7 / 1 + 0.29)' ps='2*int((1 + 2)/2) * (7 / 1 + 0.29)' nrd='0.29 / 7 ' nrs='0.29 / 7 '
+ sa=0 sb=0 sd=0 mult=1 m=1
XM1[14] VSS VG VD VD sky130_fd_pr__pfet_01v8_lvt L=0.35 W=7 nf=1 ad='int((1 + 1)/2) * 7 / 1 * 0.29' as='int((1 + 2)/2) * 7 / 1 * 0.29'
+ pd='2*int((1 + 1)/2) * (7 / 1 + 0.29)' ps='2*int((1 + 2)/2) * (7 / 1 + 0.29)' nrd='0.29 / 7 ' nrs='0.29 / 7 '
+ sa=0 sb=0 sd=0 mult=1 m=1
XM1[13] VSS VG VD VD sky130_fd_pr__pfet_01v8_lvt L=0.35 W=7 nf=1 ad='int((1 + 1)/2) * 7 / 1 * 0.29' as='int((1 + 2)/2) * 7 / 1 * 0.29'
+ pd='2*int((1 + 1)/2) * (7 / 1 + 0.29)' ps='2*int((1 + 2)/2) * (7 / 1 + 0.29)' nrd='0.29 / 7 ' nrs='0.29 / 7 '
+ sa=0 sb=0 sd=0 mult=1 m=1
XM1[12] VSS VG VD VD sky130_fd_pr__pfet_01v8_lvt L=0.35 W=7 nf=1 ad='int((1 + 1)/2) * 7 / 1 * 0.29' as='int((1 + 2)/2) * 7 / 1 * 0.29'
+ pd='2*int((1 + 1)/2) * (7 / 1 + 0.29)' ps='2*int((1 + 2)/2) * (7 / 1 + 0.29)' nrd='0.29 / 7 ' nrs='0.29 / 7 '
+ sa=0 sb=0 sd=0 mult=1 m=1
XM1[11] VSS VG VD VD sky130_fd_pr__pfet_01v8_lvt L=0.35 W=7 nf=1 ad='int((1 + 1)/2) * 7 / 1 * 0.29' as='int((1 + 2)/2) * 7 / 1 * 0.29'
+ pd='2*int((1 + 1)/2) * (7 / 1 + 0.29)' ps='2*int((1 + 2)/2) * (7 / 1 + 0.29)' nrd='0.29 / 7 ' nrs='0.29 / 7 '
+ sa=0 sb=0 sd=0 mult=1 m=1
XM1[10] VSS VG VD VD sky130_fd_pr__pfet_01v8_lvt L=0.35 W=7 nf=1 ad='int((1 + 1)/2) * 7 / 1 * 0.29' as='int((1 + 2)/2) * 7 / 1 * 0.29'
+ pd='2*int((1 + 1)/2) * (7 / 1 + 0.29)' ps='2*int((1 + 2)/2) * (7 / 1 + 0.29)' nrd='0.29 / 7 ' nrs='0.29 / 7 '
+ sa=0 sb=0 sd=0 mult=1 m=1
XM1[9] VSS VG VD VD sky130_fd_pr__pfet_01v8_lvt L=0.35 W=7 nf=1 ad='int((1 + 1)/2) * 7 / 1 * 0.29' as='int((1 + 2)/2) * 7 / 1 * 0.29'
+ pd='2*int((1 + 1)/2) * (7 / 1 + 0.29)' ps='2*int((1 + 2)/2) * (7 / 1 + 0.29)' nrd='0.29 / 7 ' nrs='0.29 / 7 '
+ sa=0 sb=0 sd=0 mult=1 m=1
XM1[8] VSS VG VD VD sky130_fd_pr__pfet_01v8_lvt L=0.35 W=7 nf=1 ad='int((1 + 1)/2) * 7 / 1 * 0.29' as='int((1 + 2)/2) * 7 / 1 * 0.29'
+ pd='2*int((1 + 1)/2) * (7 / 1 + 0.29)' ps='2*int((1 + 2)/2) * (7 / 1 + 0.29)' nrd='0.29 / 7 ' nrs='0.29 / 7 '
+ sa=0 sb=0 sd=0 mult=1 m=1
XM1[7] VSS VG VD VD sky130_fd_pr__pfet_01v8_lvt L=0.35 W=7 nf=1 ad='int((1 + 1)/2) * 7 / 1 * 0.29' as='int((1 + 2)/2) * 7 / 1 * 0.29'
+ pd='2*int((1 + 1)/2) * (7 / 1 + 0.29)' ps='2*int((1 + 2)/2) * (7 / 1 + 0.29)' nrd='0.29 / 7 ' nrs='0.29 / 7 '
+ sa=0 sb=0 sd=0 mult=1 m=1
XM1[6] VSS VG VD VD sky130_fd_pr__pfet_01v8_lvt L=0.35 W=7 nf=1 ad='int((1 + 1)/2) * 7 / 1 * 0.29' as='int((1 + 2)/2) * 7 / 1 * 0.29'
+ pd='2*int((1 + 1)/2) * (7 / 1 + 0.29)' ps='2*int((1 + 2)/2) * (7 / 1 + 0.29)' nrd='0.29 / 7 ' nrs='0.29 / 7 '
+ sa=0 sb=0 sd=0 mult=1 m=1
XM1[5] VSS VG VD VD sky130_fd_pr__pfet_01v8_lvt L=0.35 W=7 nf=1 ad='int((1 + 1)/2) * 7 / 1 * 0.29' as='int((1 + 2)/2) * 7 / 1 * 0.29'
+ pd='2*int((1 + 1)/2) * (7 / 1 + 0.29)' ps='2*int((1 + 2)/2) * (7 / 1 + 0.29)' nrd='0.29 / 7 ' nrs='0.29 / 7 '
+ sa=0 sb=0 sd=0 mult=1 m=1
XM1[4] VSS VG VD VD sky130_fd_pr__pfet_01v8_lvt L=0.35 W=7 nf=1 ad='int((1 + 1)/2) * 7 / 1 * 0.29' as='int((1 + 2)/2) * 7 / 1 * 0.29'
+ pd='2*int((1 + 1)/2) * (7 / 1 + 0.29)' ps='2*int((1 + 2)/2) * (7 / 1 + 0.29)' nrd='0.29 / 7 ' nrs='0.29 / 7 '
+ sa=0 sb=0 sd=0 mult=1 m=1
XM1[3] VSS VG VD VD sky130_fd_pr__pfet_01v8_lvt L=0.35 W=7 nf=1 ad='int((1 + 1)/2) * 7 / 1 * 0.29' as='int((1 + 2)/2) * 7 / 1 * 0.29'
+ pd='2*int((1 + 1)/2) * (7 / 1 + 0.29)' ps='2*int((1 + 2)/2) * (7 / 1 + 0.29)' nrd='0.29 / 7 ' nrs='0.29 / 7 '
+ sa=0 sb=0 sd=0 mult=1 m=1
XM1[2] VSS VG VD VD sky130_fd_pr__pfet_01v8_lvt L=0.35 W=7 nf=1 ad='int((1 + 1)/2) * 7 / 1 * 0.29' as='int((1 + 2)/2) * 7 / 1 * 0.29'
+ pd='2*int((1 + 1)/2) * (7 / 1 + 0.29)' ps='2*int((1 + 2)/2) * (7 / 1 + 0.29)' nrd='0.29 / 7 ' nrs='0.29 / 7 '
+ sa=0 sb=0 sd=0 mult=1 m=1
XM1[1] VSS VG VD VD sky130_fd_pr__pfet_01v8_lvt L=0.35 W=7 nf=1 ad='int((1 + 1)/2) * 7 / 1 * 0.29' as='int((1 + 2)/2) * 7 / 1 * 0.29'
+ pd='2*int((1 + 1)/2) * (7 / 1 + 0.29)' ps='2*int((1 + 2)/2) * (7 / 1 + 0.29)' nrd='0.29 / 7 ' nrs='0.29 / 7 '
+ sa=0 sb=0 sd=0 mult=1 m=1
XM1[0] VSS VG VD VD sky130_fd_pr__pfet_01v8_lvt L=0.35 W=7 nf=1 ad='int((1 + 1)/2) * 7 / 1 * 0.29' as='int((1 + 2)/2) * 7 / 1 * 0.29'
+ pd='2*int((1 + 1)/2) * (7 / 1 + 0.29)' ps='2*int((1 + 2)/2) * (7 / 1 + 0.29)' nrd='0.29 / 7 ' nrs='0.29 / 7 '
+ sa=0 sb=0 sd=0 mult=1 m=1
**.ends
.end
